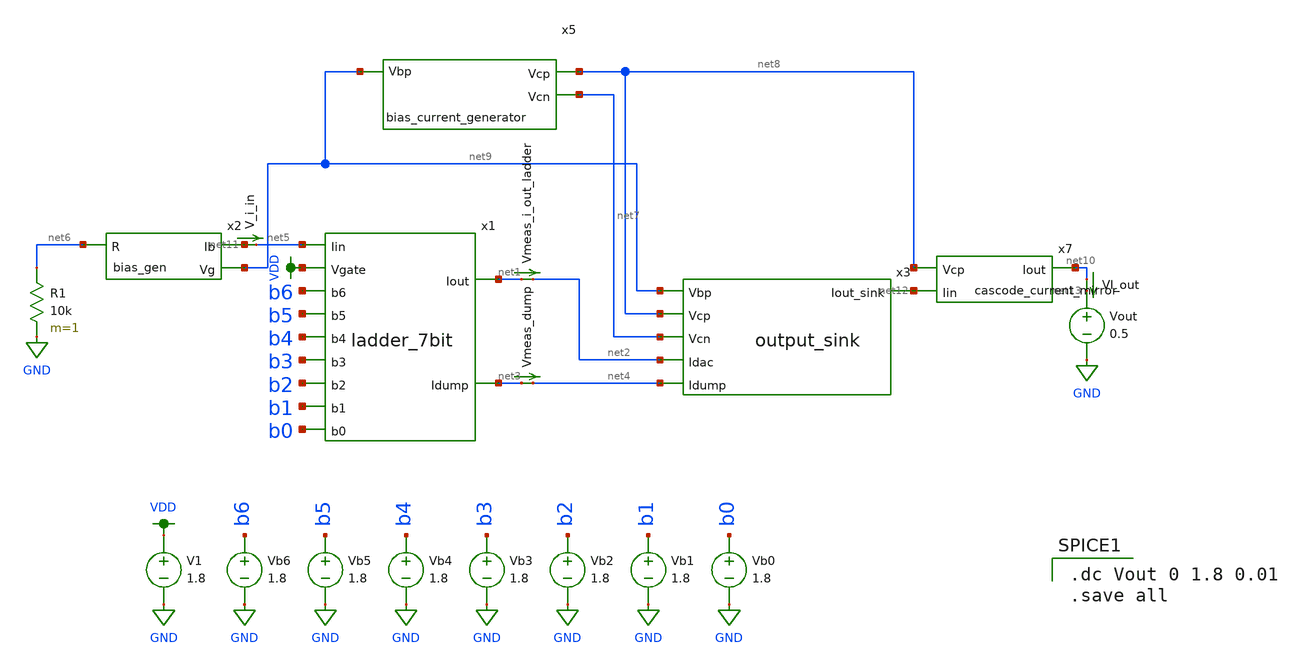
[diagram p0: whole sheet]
** sch_path: testing/test_harness_dcvout.sch
**.subckt test_harness_dcvout
Vb0 b0 GND 1.8
Vb1 b1 GND 1.8
Vb2 b2 GND 1.8
Vb3 b3 GND 1.8
Vb4 b4 GND 1.8
Vb5 b5 GND 1.8
Vb6 b6 GND 1.8
V1 VDD GND 1.8
x1 VDD net5 net3 net1 b5 b4 b1 b2 b3 b0 b6 ladder_7bit
Vmeas_i_out_ladder net1 net2 0
.save i(vmeas_i_out_ladder)
Vmeas_dump net3 net4 0
.save i(vmeas_dump)
V_i_in net11 net5 0
.save i(v_i_in)
x2 net11 net9 net6 bias_gen
R1 net6 GND 10k m=1
x5 net8 net9 net7 bias_current_generator
x3 net9 net8 net12 net7 net2 net4 output_sink
Vout net13 GND 0.5
VI_out net10 net13 0
.save i(vi_out)
x7 net12 net10 net8 cascode_current_mirror
**** begin user architecture code

.dc Vout 0 1.8 0.01
.save all


.option wnflag=1
.param MC_SWITCH=0.0
.lib ~/skywater/skywater-pdk/libraries/sky130_fd_pr_ngspice/latest/models/sky130.lib.spice tt

**** end user architecture code
**.ends

* expanding   symbol:  ../modules/ladder_7bit.sym # of pins=11
** sym_path: testing/ladder_7bit.sym
** sch_path: testing/ladder_7bit.sch
.subckt ladder_7bit Vgate Iin Idump Iout b5 b4 b1 b2 b3 b0 b6
*.opin Idump
*.opin Iout
*.ipin Vgate
*.ipin Iin
*.ipin b6
*.ipin b5
*.ipin b4
*.ipin b3
*.ipin b2
*.ipin b1
*.ipin b0
x1 Iin net8 Vgate Idump Iout net1 b6 ladder_1bit
x2 net8 net9 Vgate Idump Iout net2 b5 ladder_1bit
x3 net9 net10 Vgate Idump Iout net3 b4 ladder_1bit
x4 net10 net11 Vgate Idump Iout net4 b3 ladder_1bit
x5 net11 net12 Vgate Idump Iout net5 b2 ladder_1bit
x6 net12 net13 Vgate Idump Iout net6 b1 ladder_1bit
x7 net13 net14 Vgate Idump Iout net7 b0 ladder_1bit
XM1 Idump Vgate net14 GND sky130_fd_pr__nfet_01v8 L=0.15 W=1 nf=1 ad='int((nf+1)/2) * W/nf * 0.29' as='int((nf+2)/2) * W/nf * 0.29'
+ pd='2*int((nf+1)/2) * (W/nf + 0.29)' ps='2*int((nf+2)/2) * (W/nf + 0.29)' nrd='0.29 / W' nrs='0.29 / W'
+ sa=0 sb=0 sd=0 mult=1 m=1
X8 b6 net15 VDD GND inverter
X9 b5 net16 VDD GND inverter
X10 b4 net17 VDD GND inverter
X11 b3 net18 VDD GND inverter
X12 b2 net19 VDD GND inverter
X13 b1 net20 VDD GND inverter
X14 b0 net21 VDD GND inverter
.ends


* expanding   symbol:  ../modules/bias_gen.sym # of pins=3
** sym_path: testing/bias_gen.sym
** sch_path: testing/bias_gen.sch
.subckt bias_gen Ib Vg R
*.ipin R
*.opin Ib
*.opin Vg
XM2 R net2 net2 GND sky130_fd_pr__nfet_01v8 L=4 W=96 nf=1 ad='int((nf+1)/2) * W/nf * 0.29' as='int((nf+2)/2) * W/nf * 0.29'
+ pd='2*int((nf+1)/2) * (W/nf + 0.29)' ps='2*int((nf+2)/2) * (W/nf + 0.29)' nrd='0.29 / W' nrs='0.29 / W'
+ sa=0 sb=0 sd=0 mult=1 m=1
XM3 VDD net1 net1 VDD sky130_fd_pr__pfet_01v8 L=4 W=12 nf=1 ad='int((nf+1)/2) * W/nf * 0.29' as='int((nf+2)/2) * W/nf * 0.29'
+ pd='2*int((nf+1)/2) * (W/nf + 0.29)' ps='2*int((nf+2)/2) * (W/nf + 0.29)' nrd='0.29 / W' nrs='0.29 / W'
+ sa=0 sb=0 sd=0 mult=1 m=1
XM1 VDD Vg net2 VDD sky130_fd_pr__pfet_01v8 L=4 W=12 nf=1 ad='int((nf+1)/2) * W/nf * 0.29' as='int((nf+2)/2) * W/nf * 0.29'
+ pd='2*int((nf+1)/2) * (W/nf + 0.29)' ps='2*int((nf+2)/2) * (W/nf + 0.29)' nrd='0.29 / W' nrs='0.29 / W'
+ sa=0 sb=0 sd=0 mult=1 m=1
XM4 Vg net1 VDD VDD sky130_fd_pr__pfet_01v8 L=4 W=12 nf=1 ad='int((nf+1)/2) * W/nf * 0.29' as='int((nf+2)/2) * W/nf * 0.29'
+ pd='2*int((nf+1)/2) * (W/nf + 0.29)' ps='2*int((nf+2)/2) * (W/nf + 0.29)' nrd='0.29 / W' nrs='0.29 / W'
+ sa=0 sb=0 sd=0 mult=1 m=1
XM5 net3 Vg VDD VDD sky130_fd_pr__pfet_01v8 L=4 W=12 nf=1 ad='int((nf+1)/2) * W/nf * 0.29' as='int((nf+2)/2) * W/nf * 0.29'
+ pd='2*int((nf+1)/2) * (W/nf + 0.29)' ps='2*int((nf+2)/2) * (W/nf + 0.29)' nrd='0.29 / W' nrs='0.29 / W'
+ sa=0 sb=0 sd=0 mult=1 m=1
XM7 Ib Vg VDD VDD sky130_fd_pr__pfet_01v8 L=4 W=12 nf=1 ad='int((nf+1)/2) * W/nf * 0.29' as='int((nf+2)/2) * W/nf * 0.29'
+ pd='2*int((nf+1)/2) * (W/nf + 0.29)' ps='2*int((nf+2)/2) * (W/nf + 0.29)' nrd='0.29 / W' nrs='0.29 / W'
+ sa=0 sb=0 sd=0 mult=1 m=1
XM6 net1 net2 GND GND sky130_fd_pr__nfet_01v8 L=4 W=12 nf=1 ad='int((nf+1)/2) * W/nf * 0.29' as='int((nf+2)/2) * W/nf * 0.29'
+ pd='2*int((nf+1)/2) * (W/nf + 0.29)' ps='2*int((nf+2)/2) * (W/nf + 0.29)' nrd='0.29 / W' nrs='0.29 / W'
+ sa=0 sb=0 sd=0 mult=1 m=1
XM8 GND net3 Vg GND sky130_fd_pr__nfet_01v8 L=4 W=12 nf=1 ad='int((nf+1)/2) * W/nf * 0.29' as='int((nf+2)/2) * W/nf * 0.29'
+ pd='2*int((nf+1)/2) * (W/nf + 0.29)' ps='2*int((nf+2)/2) * (W/nf + 0.29)' nrd='0.29 / W' nrs='0.29 / W'
+ sa=0 sb=0 sd=0 mult=1 m=1
XM9 net3 net3 GND GND sky130_fd_pr__nfet_01v8 L=4 W=12 nf=1 ad='int((nf+1)/2) * W/nf * 0.29' as='int((nf+2)/2) * W/nf * 0.29'
+ pd='2*int((nf+1)/2) * (W/nf + 0.29)' ps='2*int((nf+2)/2) * (W/nf + 0.29)' nrd='0.29 / W' nrs='0.29 / W'
+ sa=0 sb=0 sd=0 mult=1 m=1
.ends


* expanding   symbol:  ../modules/bias_current_generator.sym # of pins=3
** sym_path: testing/bias_current_generator.sym
** sch_path: testing/bias_current_generator.sch
.subckt bias_current_generator Vcp Vbp Vcn
*.opin Vcn
*.opin Vcp
*.ipin Vbp
XM4 Vcn Vbp VDD VDD sky130_fd_pr__pfet_01v8 L=0.5 W=12 nf=1 ad='int((nf+1)/2) * W/nf * 0.29' as='int((nf+2)/2) * W/nf * 0.29'
+ pd='2*int((nf+1)/2) * (W/nf + 0.29)' ps='2*int((nf+2)/2) * (W/nf + 0.29)' nrd='0.29 / W' nrs='0.29 / W'
+ sa=0 sb=0 sd=0 mult=1 m=1
XM11 Vcn Vcn net2 GND sky130_fd_pr__nfet_01v8 L=0.5 W=12 nf=1 ad='int((nf+1)/2) * W/nf * 0.29' as='int((nf+2)/2) * W/nf * 0.29'
+ pd='2*int((nf+1)/2) * (W/nf + 0.29)' ps='2*int((nf+2)/2) * (W/nf + 0.29)' nrd='0.29 / W' nrs='0.29 / W'
+ sa=0 sb=0 sd=0 mult=1 m=1
XM8 net5 net5 net2 GND sky130_fd_pr__nfet_01v8 L=0.5 W=12 nf=1 ad='int((nf+1)/2) * W/nf * 0.29' as='int((nf+2)/2) * W/nf * 0.29'
+ pd='2*int((nf+1)/2) * (W/nf + 0.29)' ps='2*int((nf+2)/2) * (W/nf + 0.29)' nrd='0.29 / W' nrs='0.29 / W'
+ sa=0 sb=0 sd=0 mult=1 m=1
XM9 net2 net5 net5 GND sky130_fd_pr__nfet_01v8 L=0.5 W=12 nf=1 ad='int((nf+1)/2) * W/nf * 0.29' as='int((nf+2)/2) * W/nf * 0.29'
+ pd='2*int((nf+1)/2) * (W/nf + 0.29)' ps='2*int((nf+2)/2) * (W/nf + 0.29)' nrd='0.29 / W' nrs='0.29 / W'
+ sa=0 sb=0 sd=0 mult=1 m=1
XM10 net5 net5 net2 GND sky130_fd_pr__nfet_01v8 L=0.5 W=12 nf=1 ad='int((nf+1)/2) * W/nf * 0.29' as='int((nf+2)/2) * W/nf * 0.29'
+ pd='2*int((nf+1)/2) * (W/nf + 0.29)' ps='2*int((nf+2)/2) * (W/nf + 0.29)' nrd='0.29 / W' nrs='0.29 / W'
+ sa=0 sb=0 sd=0 mult=1 m=1
XM22 net2 net5 net5 GND sky130_fd_pr__nfet_01v8 L=0.5 W=12 nf=1 ad='int((nf+1)/2) * W/nf * 0.29' as='int((nf+2)/2) * W/nf * 0.29'
+ pd='2*int((nf+1)/2) * (W/nf + 0.29)' ps='2*int((nf+2)/2) * (W/nf + 0.29)' nrd='0.29 / W' nrs='0.29 / W'
+ sa=0 sb=0 sd=0 mult=1 m=1
XM23 GND net5 net2 GND sky130_fd_pr__nfet_01v8 L=0.5 W=12 nf=1 ad='int((nf+1)/2) * W/nf * 0.29' as='int((nf+2)/2) * W/nf * 0.29'
+ pd='2*int((nf+1)/2) * (W/nf + 0.29)' ps='2*int((nf+2)/2) * (W/nf + 0.29)' nrd='0.29 / W' nrs='0.29 / W'
+ sa=0 sb=0 sd=0 mult=1 m=1
XM28 Vcp net1 GND GND sky130_fd_pr__nfet_01v8 L=0.5 W=12 nf=1 ad='int((nf+1)/2) * W/nf * 0.29' as='int((nf+2)/2) * W/nf * 0.29'
+ pd='2*int((nf+1)/2) * (W/nf + 0.29)' ps='2*int((nf+2)/2) * (W/nf + 0.29)' nrd='0.29 / W' nrs='0.29 / W'
+ sa=0 sb=0 sd=0 mult=1 m=1
XM12 GND net1 net7 GND sky130_fd_pr__nfet_01v8 L=0.5 W=12 nf=1 ad='int((nf+1)/2) * W/nf * 0.29' as='int((nf+2)/2) * W/nf * 0.29'
+ pd='2*int((nf+1)/2) * (W/nf + 0.29)' ps='2*int((nf+2)/2) * (W/nf + 0.29)' nrd='0.29 / W' nrs='0.29 / W'
+ sa=0 sb=0 sd=0 mult=1 m=1
XM13 net7 net1 net8 GND sky130_fd_pr__nfet_01v8 L=0.5 W=12 nf=1 ad='int((nf+1)/2) * W/nf * 0.29' as='int((nf+2)/2) * W/nf * 0.29'
+ pd='2*int((nf+1)/2) * (W/nf + 0.29)' ps='2*int((nf+2)/2) * (W/nf + 0.29)' nrd='0.29 / W' nrs='0.29 / W'
+ sa=0 sb=0 sd=0 mult=1 m=1
XM14 net8 net1 net13 GND sky130_fd_pr__nfet_01v8 L=0.5 W=12 nf=1 ad='int((nf+1)/2) * W/nf * 0.29' as='int((nf+2)/2) * W/nf * 0.29'
+ pd='2*int((nf+1)/2) * (W/nf + 0.29)' ps='2*int((nf+2)/2) * (W/nf + 0.29)' nrd='0.29 / W' nrs='0.29 / W'
+ sa=0 sb=0 sd=0 mult=1 m=1
XM15 net13 net1 net12 GND sky130_fd_pr__nfet_01v8 L=0.5 W=12 nf=1 ad='int((nf+1)/2) * W/nf * 0.29' as='int((nf+2)/2) * W/nf * 0.29'
+ pd='2*int((nf+1)/2) * (W/nf + 0.29)' ps='2*int((nf+2)/2) * (W/nf + 0.29)' nrd='0.29 / W' nrs='0.29 / W'
+ sa=0 sb=0 sd=0 mult=1 m=1
XM24 net12 net1 net10 GND sky130_fd_pr__nfet_01v8 L=0.5 W=12 nf=1 ad='int((nf+1)/2) * W/nf * 0.29' as='int((nf+2)/2) * W/nf * 0.29'
+ pd='2*int((nf+1)/2) * (W/nf + 0.29)' ps='2*int((nf+2)/2) * (W/nf + 0.29)' nrd='0.29 / W' nrs='0.29 / W'
+ sa=0 sb=0 sd=0 mult=1 m=1
XM5 VDD Vbp net3 VDD sky130_fd_pr__pfet_01v8 L=0.5 W=12 nf=1 ad='int((nf+1)/2) * W/nf * 0.29' as='int((nf+2)/2) * W/nf * 0.29'
+ pd='2*int((nf+1)/2) * (W/nf + 0.29)' ps='2*int((nf+2)/2) * (W/nf + 0.29)' nrd='0.29 / W' nrs='0.29 / W'
+ sa=0 sb=0 sd=0 mult=1 m=1
XM6 net3 Vbp net4 VDD sky130_fd_pr__pfet_01v8 L=0.5 W=12 nf=1 ad='int((nf+1)/2) * W/nf * 0.29' as='int((nf+2)/2) * W/nf * 0.29'
+ pd='2*int((nf+1)/2) * (W/nf + 0.29)' ps='2*int((nf+2)/2) * (W/nf + 0.29)' nrd='0.29 / W' nrs='0.29 / W'
+ sa=0 sb=0 sd=0 mult=1 m=1
XM7 net4 Vbp net6 VDD sky130_fd_pr__pfet_01v8 L=0.5 W=12 nf=1 ad='int((nf+1)/2) * W/nf * 0.29' as='int((nf+2)/2) * W/nf * 0.29'
+ pd='2*int((nf+1)/2) * (W/nf + 0.29)' ps='2*int((nf+2)/2) * (W/nf + 0.29)' nrd='0.29 / W' nrs='0.29 / W'
+ sa=0 sb=0 sd=0 mult=1 m=1
XM20 net6 Vbp net11 VDD sky130_fd_pr__pfet_01v8 L=0.5 W=12 nf=1 ad='int((nf+1)/2) * W/nf * 0.29' as='int((nf+2)/2) * W/nf * 0.29'
+ pd='2*int((nf+1)/2) * (W/nf + 0.29)' ps='2*int((nf+2)/2) * (W/nf + 0.29)' nrd='0.29 / W' nrs='0.29 / W'
+ sa=0 sb=0 sd=0 mult=1 m=1
XM21 net11 Vbp net5 VDD sky130_fd_pr__pfet_01v8 L=0.5 W=12 nf=1 ad='int((nf+1)/2) * W/nf * 0.29' as='int((nf+2)/2) * W/nf * 0.29'
+ pd='2*int((nf+1)/2) * (W/nf + 0.29)' ps='2*int((nf+2)/2) * (W/nf + 0.29)' nrd='0.29 / W' nrs='0.29 / W'
+ sa=0 sb=0 sd=0 mult=1 m=1
XM16 Vcp Vcp net9 VDD sky130_fd_pr__pfet_01v8 L=0.5 W=12 nf=1 ad='int((nf+1)/2) * W/nf * 0.29' as='int((nf+2)/2) * W/nf * 0.29'
+ pd='2*int((nf+1)/2) * (W/nf + 0.29)' ps='2*int((nf+2)/2) * (W/nf + 0.29)' nrd='0.29 / W' nrs='0.29 / W'
+ sa=0 sb=0 sd=0 mult=1 m=1
XM17 net10 net10 net9 VDD sky130_fd_pr__pfet_01v8 L=0.5 W=12 nf=1 ad='int((nf+1)/2) * W/nf * 0.29' as='int((nf+2)/2) * W/nf * 0.29'
+ pd='2*int((nf+1)/2) * (W/nf + 0.29)' ps='2*int((nf+2)/2) * (W/nf + 0.29)' nrd='0.29 / W' nrs='0.29 / W'
+ sa=0 sb=0 sd=0 mult=1 m=1
XM18 net9 net10 net10 VDD sky130_fd_pr__pfet_01v8 L=0.5 W=12 nf=1 ad='int((nf+1)/2) * W/nf * 0.29' as='int((nf+2)/2) * W/nf * 0.29'
+ pd='2*int((nf+1)/2) * (W/nf + 0.29)' ps='2*int((nf+2)/2) * (W/nf + 0.29)' nrd='0.29 / W' nrs='0.29 / W'
+ sa=0 sb=0 sd=0 mult=1 m=1
XM19 net10 net10 net9 VDD sky130_fd_pr__pfet_01v8 L=0.5 W=12 nf=1 ad='int((nf+1)/2) * W/nf * 0.29' as='int((nf+2)/2) * W/nf * 0.29'
+ pd='2*int((nf+1)/2) * (W/nf + 0.29)' ps='2*int((nf+2)/2) * (W/nf + 0.29)' nrd='0.29 / W' nrs='0.29 / W'
+ sa=0 sb=0 sd=0 mult=1 m=1
XM25 net9 net10 net10 VDD sky130_fd_pr__pfet_01v8 L=0.5 W=12 nf=1 ad='int((nf+1)/2) * W/nf * 0.29' as='int((nf+2)/2) * W/nf * 0.29'
+ pd='2*int((nf+1)/2) * (W/nf + 0.29)' ps='2*int((nf+2)/2) * (W/nf + 0.29)' nrd='0.29 / W' nrs='0.29 / W'
+ sa=0 sb=0 sd=0 mult=1 m=1
XM26 VDD net10 net9 VDD sky130_fd_pr__pfet_01v8 L=0.5 W=12 nf=1 ad='int((nf+1)/2) * W/nf * 0.29' as='int((nf+2)/2) * W/nf * 0.29'
+ pd='2*int((nf+1)/2) * (W/nf + 0.29)' ps='2*int((nf+2)/2) * (W/nf + 0.29)' nrd='0.29 / W' nrs='0.29 / W'
+ sa=0 sb=0 sd=0 mult=1 m=1
XM2 net1 Vbp VDD VDD sky130_fd_pr__pfet_01v8 L=0.5 W=12 nf=1 ad='int((nf+1)/2) * W/nf * 0.29' as='int((nf+2)/2) * W/nf * 0.29'
+ pd='2*int((nf+1)/2) * (W/nf + 0.29)' ps='2*int((nf+2)/2) * (W/nf + 0.29)' nrd='0.29 / W' nrs='0.29 / W'
+ sa=0 sb=0 sd=0 mult=1 m=1
XM3 net1 net1 GND GND sky130_fd_pr__nfet_01v8 L=0.5 W=12 nf=1 ad='int((nf+1)/2) * W/nf * 0.29' as='int((nf+2)/2) * W/nf * 0.29'
+ pd='2*int((nf+1)/2) * (W/nf + 0.29)' ps='2*int((nf+2)/2) * (W/nf + 0.29)' nrd='0.29 / W' nrs='0.29 / W'
+ sa=0 sb=0 sd=0 mult=1 m=1
.ends


* expanding   symbol:  ../modules/output_sink.sym # of pins=6
** sym_path: testing/output_sink.sym
** sch_path: testing/output_sink.sch
.subckt output_sink Vbp Vcp Iout_sink Vcn Idac Idump
*.ipin Idump
*.ipin Idac
*.ipin Vcn
*.ipin Vcp
*.ipin Vbp
*.opin Iout_sink
XM1 net1 Vcn Idump GND sky130_fd_pr__nfet_01v8 L=0.5 W=12 nf=1 ad='int((nf+1)/2) * W/nf * 0.29' as='int((nf+2)/2) * W/nf * 0.29'
+ pd='2*int((nf+1)/2) * (W/nf + 0.29)' ps='2*int((nf+2)/2) * (W/nf + 0.29)' nrd='0.29 / W' nrs='0.29 / W'
+ sa=0 sb=0 sd=0 mult=1 m=1
XM8 net4 Vbp VDD VDD sky130_fd_pr__pfet_01v8 L=0.5 W=12 nf=1 ad='int((nf+1)/2) * W/nf * 0.29' as='int((nf+2)/2) * W/nf * 0.29'
+ pd='2*int((nf+1)/2) * (W/nf + 0.29)' ps='2*int((nf+2)/2) * (W/nf + 0.29)' nrd='0.29 / W' nrs='0.29 / W'
+ sa=0 sb=0 sd=0 mult=1 m=1
XM7 net5 Vbp VDD VDD sky130_fd_pr__pfet_01v8 L=0.5 W=12 nf=1 ad='int((nf+1)/2) * W/nf * 0.29' as='int((nf+2)/2) * W/nf * 0.29'
+ pd='2*int((nf+1)/2) * (W/nf + 0.29)' ps='2*int((nf+2)/2) * (W/nf + 0.29)' nrd='0.29 / W' nrs='0.29 / W'
+ sa=0 sb=0 sd=0 mult=1 m=1
XM9 net6 Vbp VDD VDD sky130_fd_pr__pfet_01v8 L=0.5 W=12 nf=1 ad='int((nf+1)/2) * W/nf * 0.29' as='int((nf+2)/2) * W/nf * 0.29'
+ pd='2*int((nf+1)/2) * (W/nf + 0.29)' ps='2*int((nf+2)/2) * (W/nf + 0.29)' nrd='0.29 / W' nrs='0.29 / W'
+ sa=0 sb=0 sd=0 mult=1 m=1
XM10 Iout_sink Vcp net6 VDD sky130_fd_pr__pfet_01v8 L=0.5 W=12 nf=1 ad='int((nf+1)/2) * W/nf * 0.29'
+ as='int((nf+2)/2) * W/nf * 0.29' pd='2*int((nf+1)/2) * (W/nf + 0.29)' ps='2*int((nf+2)/2) * (W/nf + 0.29)'
+ nrd='0.29 / W' nrs='0.29 / W' sa=0 sb=0 sd=0 mult=1 m=1
XM11 net2 Vcp net5 VDD sky130_fd_pr__pfet_01v8 L=0.5 W=12 nf=1 ad='int((nf+1)/2) * W/nf * 0.29' as='int((nf+2)/2) * W/nf * 0.29'
+ pd='2*int((nf+1)/2) * (W/nf + 0.29)' ps='2*int((nf+2)/2) * (W/nf + 0.29)' nrd='0.29 / W' nrs='0.29 / W'
+ sa=0 sb=0 sd=0 mult=1 m=1
XM12 net1 Vcp net4 VDD sky130_fd_pr__pfet_01v8 L=0.5 W=12 nf=1 ad='int((nf+1)/2) * W/nf * 0.29' as='int((nf+2)/2) * W/nf * 0.29'
+ pd='2*int((nf+1)/2) * (W/nf + 0.29)' ps='2*int((nf+2)/2) * (W/nf + 0.29)' nrd='0.29 / W' nrs='0.29 / W'
+ sa=0 sb=0 sd=0 mult=1 m=1
XM3 net2 Vcn Idac GND sky130_fd_pr__nfet_01v8 L=0.5 W=12 nf=1 ad='int((nf+1)/2) * W/nf * 0.29' as='int((nf+2)/2) * W/nf * 0.29'
+ pd='2*int((nf+1)/2) * (W/nf + 0.29)' ps='2*int((nf+2)/2) * (W/nf + 0.29)' nrd='0.29 / W' nrs='0.29 / W'
+ sa=0 sb=0 sd=0 mult=1 m=1
XM5 Iout_sink Vcn net3 GND sky130_fd_pr__nfet_01v8 L=0.5 W=12 nf=1 ad='int((nf+1)/2) * W/nf * 0.29' as='int((nf+2)/2) * W/nf * 0.29'
+ pd='2*int((nf+1)/2) * (W/nf + 0.29)' ps='2*int((nf+2)/2) * (W/nf + 0.29)' nrd='0.29 / W' nrs='0.29 / W'
+ sa=0 sb=0 sd=0 mult=1 m=1
XM6 net3 net2 GND GND sky130_fd_pr__nfet_01v8 L=0.5 W=12 nf=1 ad='int((nf+1)/2) * W/nf * 0.29' as='int((nf+2)/2) * W/nf * 0.29'
+ pd='2*int((nf+1)/2) * (W/nf + 0.29)' ps='2*int((nf+2)/2) * (W/nf + 0.29)' nrd='0.29 / W' nrs='0.29 / W'
+ sa=0 sb=0 sd=0 mult=1 m=1
XM13 Idac net2 GND GND sky130_fd_pr__nfet_01v8 L=0.5 W=12 nf=1 ad='int((nf+1)/2) * W/nf * 0.29' as='int((nf+2)/2) * W/nf * 0.29'
+ pd='2*int((nf+1)/2) * (W/nf + 0.29)' ps='2*int((nf+2)/2) * (W/nf + 0.29)' nrd='0.29 / W' nrs='0.29 / W'
+ sa=0 sb=0 sd=0 mult=1 m=1
XM14 Idump net1 GND GND sky130_fd_pr__nfet_01v8 L=0.5 W=12 nf=1 ad='int((nf+1)/2) * W/nf * 0.29' as='int((nf+2)/2) * W/nf * 0.29'
+ pd='2*int((nf+1)/2) * (W/nf + 0.29)' ps='2*int((nf+2)/2) * (W/nf + 0.29)' nrd='0.29 / W' nrs='0.29 / W'
+ sa=0 sb=0 sd=0 mult=1 m=1
.ends


* expanding   symbol:  /home/madvlsi/Documents/R2R-DAC/modules/cascode_current_mirror.sym # of
*+ pins=3
** sym_path: modules/cascode_current_mirror.sym
** sch_path: modules/cascode_current_mirror.sch
.subckt cascode_current_mirror Iin Iout Vcp
*.ipin Vcp
*.ipin Iin
*.opin Iout
XM5 net1 Iin VDD VDD sky130_fd_pr__pfet_01v8 L=8 W=24 nf=1 ad='int((nf+1)/2) * W/nf * 0.29' as='int((nf+2)/2) * W/nf * 0.29'
+ pd='2*int((nf+1)/2) * (W/nf + 0.29)' ps='2*int((nf+2)/2) * (W/nf + 0.29)' nrd='0.29 / W' nrs='0.29 / W'
+ sa=0 sb=0 sd=0 mult=1 m=1
XM1 Iin Vcp net1 VDD sky130_fd_pr__pfet_01v8 L=8 W=24 nf=1 ad='int((nf+1)/2) * W/nf * 0.29' as='int((nf+2)/2) * W/nf * 0.29'
+ pd='2*int((nf+1)/2) * (W/nf + 0.29)' ps='2*int((nf+2)/2) * (W/nf + 0.29)' nrd='0.29 / W' nrs='0.29 / W'
+ sa=0 sb=0 sd=0 mult=1 m=1
XM2 net2 Iin VDD VDD sky130_fd_pr__pfet_01v8 L=8 W=24 nf=1 ad='int((nf+1)/2) * W/nf * 0.29' as='int((nf+2)/2) * W/nf * 0.29'
+ pd='2*int((nf+1)/2) * (W/nf + 0.29)' ps='2*int((nf+2)/2) * (W/nf + 0.29)' nrd='0.29 / W' nrs='0.29 / W'
+ sa=0 sb=0 sd=0 mult=1 m=1
XM3 Iout Vcp net2 VDD sky130_fd_pr__pfet_01v8 L=8 W=24 nf=1 ad='int((nf+1)/2) * W/nf * 0.29' as='int((nf+2)/2) * W/nf * 0.29'
+ pd='2*int((nf+1)/2) * (W/nf + 0.29)' ps='2*int((nf+2)/2) * (W/nf + 0.29)' nrd='0.29 / W' nrs='0.29 / W'
+ sa=0 sb=0 sd=0 mult=1 m=1
.ends


* expanding   symbol:  /home/madvlsi/R2R-DAC/ladder_1bit.sym # of pins=7
** sym_path: testing/ladder_1bit.sym
** sch_path: testing/ladder_1bit.sch
.subckt ladder_1bit Iin_in Iin_out Vg I_dump Iout B_bar B
*.ipin Iin_in
*.ipin Vg
*.ipin B
*.ipin B_bar
*.opin Iin_out
*.opin I_dump
*.opin Iout
XM5 net1 Vg Iin_in GND sky130_fd_pr__nfet_01v8 L=0.15 W=1 nf=1 ad='int((nf+1)/2) * W/nf * 0.29' as='int((nf+2)/2) * W/nf * 0.29'
+ pd='2*int((nf+1)/2) * (W/nf + 0.29)' ps='2*int((nf+2)/2) * (W/nf + 0.29)' nrd='0.29 / W' nrs='0.29 / W'
+ sa=0 sb=0 sd=0 mult=1 m=1
XM6 Iout B net1 GND sky130_fd_pr__nfet_01v8 L=0.15 W=1 nf=1 ad='int((nf+1)/2) * W/nf * 0.29' as='int((nf+2)/2) * W/nf * 0.29'
+ pd='2*int((nf+1)/2) * (W/nf + 0.29)' ps='2*int((nf+2)/2) * (W/nf + 0.29)' nrd='0.29 / W' nrs='0.29 / W'
+ sa=0 sb=0 sd=0 mult=1 m=1
XM7 net1 B_bar I_dump GND sky130_fd_pr__nfet_01v8 L=0.15 W=1 nf=1 ad='int((nf+1)/2) * W/nf * 0.29' as='int((nf+2)/2) * W/nf * 0.29'
+ pd='2*int((nf+1)/2) * (W/nf + 0.29)' ps='2*int((nf+2)/2) * (W/nf + 0.29)' nrd='0.29 / W' nrs='0.29 / W'
+ sa=0 sb=0 sd=0 mult=1 m=1
XM8 Iin_in Vg Iin_out GND sky130_fd_pr__nfet_01v8 L=0.15 W=1 nf=1 ad='int((nf+1)/2) * W/nf * 0.29' as='int((nf+2)/2) * W/nf * 0.29'
+ pd='2*int((nf+1)/2) * (W/nf + 0.29)' ps='2*int((nf+2)/2) * (W/nf + 0.29)' nrd='0.29 / W' nrs='0.29 / W'
+ sa=0 sb=0 sd=0 mult=1 m=1
.ends


* expanding   symbol:  /home/madvlsi/Documents/mp1/inverter.sym # of pins=4
** sym_path: /home/madvlsi/Documents/mp1/inverter.sym
** sch_path: /home/madvlsi/Documents/mp1/inverter.sch
.subckt inverter A Y VP VN
*.ipin A
*.iopin VP
*.iopin VN
*.opin Y
XM3 Y A VP VP sky130_fd_pr__pfet_01v8 L=0.15 W=1 nf=1 ad='int((nf+1)/2) * W/nf * 0.29' as='int((nf+2)/2) * W/nf * 0.29'
+ pd='2*int((nf+1)/2) * (W/nf + 0.29)' ps='2*int((nf+2)/2) * (W/nf + 0.29)' nrd='0.29 / W' nrs='0.29 / W'
+ sa=0 sb=0 sd=0 mult=1 m=1
XM4 Y A VN VN sky130_fd_pr__nfet_01v8 L=0.15 W=1 nf=1 ad='int((nf+1)/2) * W/nf * 0.29' as='int((nf+2)/2) * W/nf * 0.29'
+ pd='2*int((nf+1)/2) * (W/nf + 0.29)' ps='2*int((nf+2)/2) * (W/nf + 0.29)' nrd='0.29 / W' nrs='0.29 / W'
+ sa=0 sb=0 sd=0 mult=1 m=1
.ends

.GLOBAL GND
.GLOBAL VDD
.end
